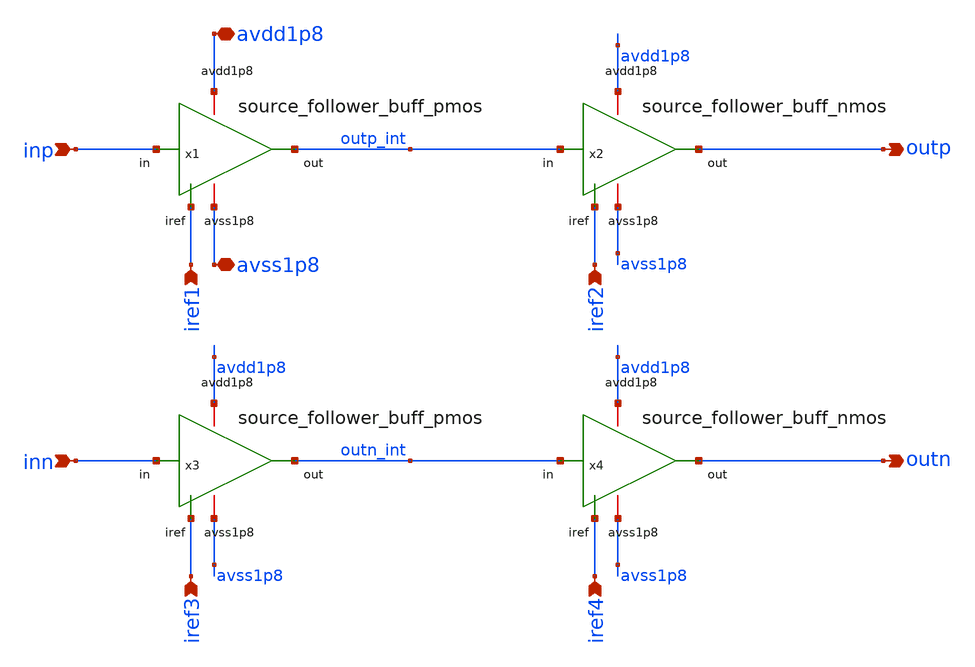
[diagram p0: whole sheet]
** sch_path: xschem/afernandez_residue_amplifier/source_follower_buff_diff.sch
**.subckt source_follower_buff_diff avdd1p8 avss1p8 outp outn inp inn iref1 iref2 iref3 iref4
*.iopin avdd1p8
*.iopin avss1p8
*.opin outp
*.opin outn
*.ipin inp
*.ipin inn
*.ipin iref1
*.ipin iref2
*.ipin iref3
*.ipin iref4
x1 avdd1p8 iref1 inp outp_int avss1p8 source_follower_buff_pmos
x2 avdd1p8 iref2 outp_int outp avss1p8 source_follower_buff_nmos
x3 avdd1p8 iref3 inn outn_int avss1p8 source_follower_buff_pmos
x4 avdd1p8 iref4 outn_int outn avss1p8 source_follower_buff_nmos
**.ends
.end
